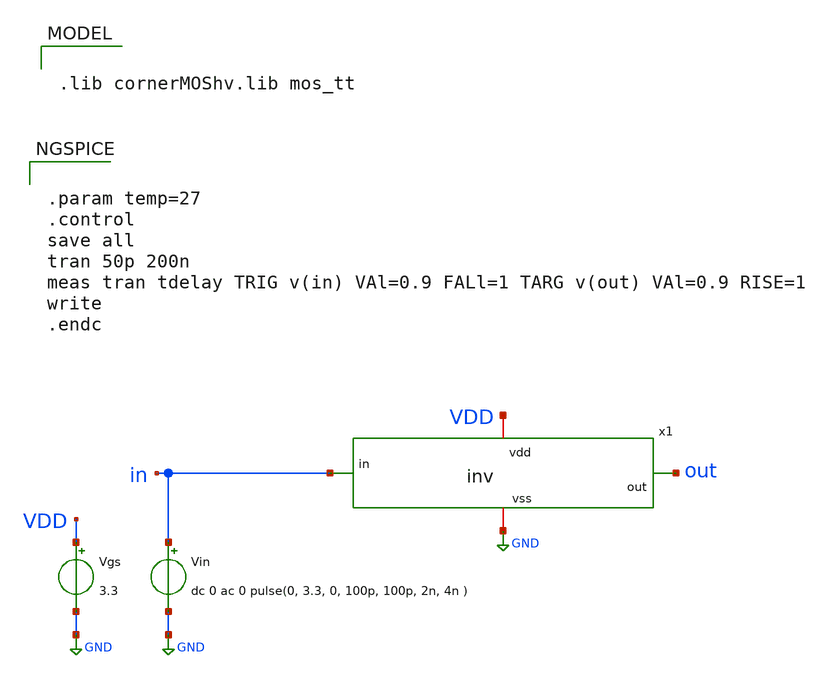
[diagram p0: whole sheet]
** sch_path: ChipUSM_AnalogTrack24/inv/tb_inv.sch
**.subckt tb_inv
Vgs VDD GND 3.3
Vin in GND dc 0 ac 0 pulse(0, 3.3, 0, 100p, 100p, 2n, 4n )
x1 VDD GND in out inv
**** begin user architecture code


.lib cornerMOShv.lib mos_tt




.param temp=27
.control
save all
tran 50p 200n
meas tran tdelay TRIG v(in) VAl=0.9 FALl=1 TARG v(out) VAl=0.9 RISE=1
write
.endc


**** end user architecture code
**.ends

* expanding   symbol:  inv.sym # of pins=4
** sym_path: ChipUSM_AnalogTrack24/inv/inv.sym
** sch_path: ChipUSM_AnalogTrack24/inv/inv.sch
.subckt inv vdd vss in out
*.iopin vdd
*.iopin vss
*.ipin in
*.opin out
XM1 vss in out vss sg13_hv_nmos w=5u l=0.22u ng=1 m=54 mm_ok=1
XM2 out in vdd vdd sg13_hv_pmos w=5u l=0.22u ng=1 m=54 mm_ok=1
.ends

.GLOBAL GND
.end
